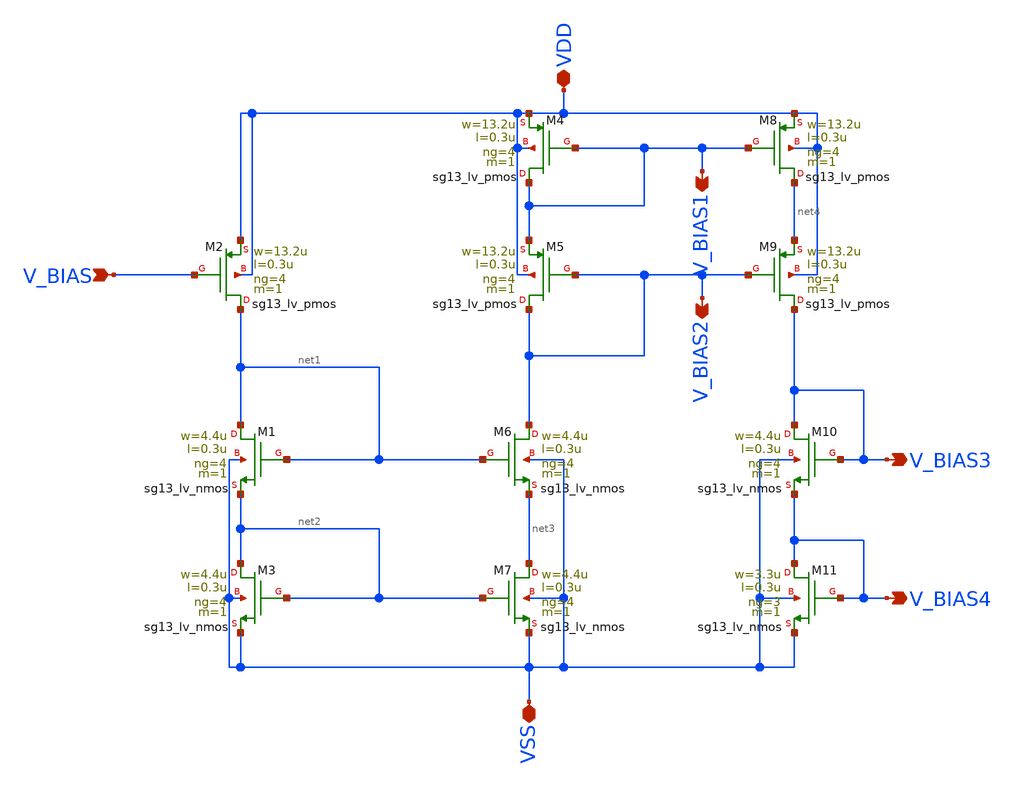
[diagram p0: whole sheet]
** sch_path: two-stage-ota-with-cmfb/Layout_PEX_PostSimulation/LAYOUT/SCHEMATIC_FOR_LAYOUT/BIAS_Block/BIAS_Block.sch
**.subckt BIAS_Block VSS V_BIAS4 V_BIAS2 V_BIAS3 VDD V_BIAS1 V_BIAS
*.iopin VSS
*.opin V_BIAS4
*.opin V_BIAS2
*.opin V_BIAS3
*.iopin VDD
*.opin V_BIAS1
*.ipin V_BIAS
XM1 net1 net1 net2 VSS sg13_lv_nmos w=4.4u l=0.3u ng=4 m=1 mm_ok=1
XM9 V_BIAS3 V_BIAS2 net4 VDD sg13_lv_pmos w=13.2u l=0.3u ng=4 m=1 mm_ok=1
XM10 V_BIAS3 V_BIAS3 V_BIAS4 VSS sg13_lv_nmos w=4.4u l=0.3u ng=4 m=1 mm_ok=1
XM11 V_BIAS4 V_BIAS4 VSS VSS sg13_lv_nmos w=3.3u l=0.3u ng=3 m=1 mm_ok=1
XM8 net4 V_BIAS1 VDD VDD sg13_lv_pmos w=13.2u l=0.3u ng=4 m=1 mm_ok=1
XM6 V_BIAS2 net1 net3 VSS sg13_lv_nmos w=4.4u l=0.3u ng=4 m=1 mm_ok=1
XM2 net1 V_BIAS VDD VDD sg13_lv_pmos w=13.2u l=0.3u ng=4 m=1 mm_ok=1
XM7 net3 net2 VSS VSS sg13_lv_nmos w=4.4u l=0.3u ng=4 m=1 mm_ok=1
XM4 V_BIAS1 V_BIAS1 VDD VDD sg13_lv_pmos w=13.2u l=0.3u ng=4 m=1 mm_ok=1
XM5 V_BIAS2 V_BIAS2 V_BIAS1 VDD sg13_lv_pmos w=13.2u l=0.3u ng=4 m=1 mm_ok=1
XM3 net2 net2 VSS VSS sg13_lv_nmos w=4.4u l=0.3u ng=4 m=1 mm_ok=1
**.ends
.end
